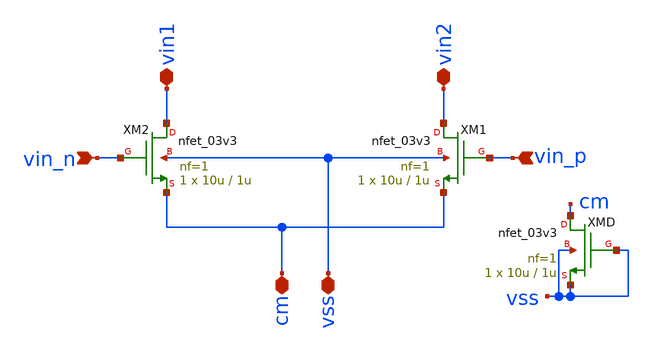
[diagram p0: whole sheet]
** sch_path: LDO/xschem/diff_pair/symbol/diff_pair.sch
**.subckt diff_pair vin_n vin_p vss vin1 vin2 cm
*.ipin vin_n
*.ipin vin_p
*.iopin vss
*.iopin vin1
*.iopin vin2
*.iopin cm
XM2 vin1 vin_n cm vss nfet_03v3 L=1u W=10u nf=1 ad='int((nf+1)/2) * W/nf * 0.18u' as='int((nf+2)/2) * W/nf * 0.18u'
+ pd='2*int((nf+1)/2) * (W/nf + 0.18u)' ps='2*int((nf+2)/2) * (W/nf + 0.18u)' nrd='0.18u / W' nrs='0.18u / W'
+ sa=0 sb=0 sd=0 m=1
XM1 vin2 vin_p cm vss nfet_03v3 L=1u W=10u nf=1 ad='int((nf+1)/2) * W/nf * 0.18u' as='int((nf+2)/2) * W/nf * 0.18u'
+ pd='2*int((nf+1)/2) * (W/nf + 0.18u)' ps='2*int((nf+2)/2) * (W/nf + 0.18u)' nrd='0.18u / W' nrs='0.18u / W'
+ sa=0 sb=0 sd=0 m=1
XMD cm vss vss vss nfet_03v3 L=1u W=10u nf=1 ad='int((nf+1)/2) * W/nf * 0.18u' as='int((nf+2)/2) * W/nf * 0.18u'
+ pd='2*int((nf+1)/2) * (W/nf + 0.18u)' ps='2*int((nf+2)/2) * (W/nf + 0.18u)' nrd='0.18u / W' nrs='0.18u / W'
+ sa=0 sb=0 sd=0 m=1
**.ends
.end
